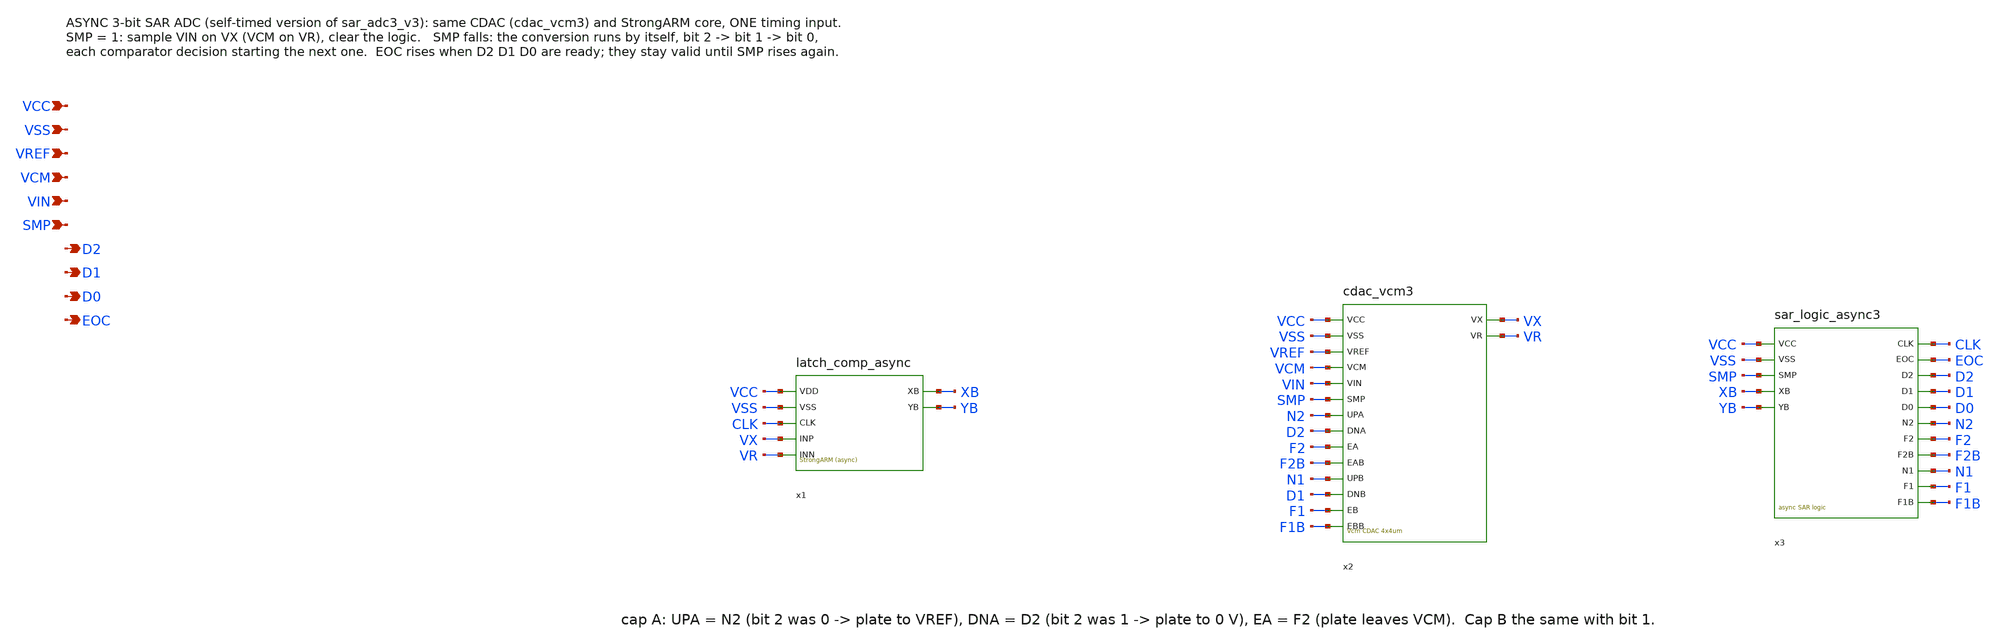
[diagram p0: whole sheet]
** sch_path: SAR_improved/sar_adc3_async.sch
**.subckt sar_adc3_async VCC VSS VREF VCM VIN SMP D2 D1 D0 EOC
*.ipin VCC
*.ipin VSS
*.ipin VREF
*.ipin VCM
*.ipin VIN
*.ipin SMP
*.opin D2
*.opin D1
*.opin D0
*.opin EOC
x1 VCC VSS CLK VX VR XB YB latch_comp_async
x2 VCC VSS VREF VCM VIN SMP N2 D2 F2 F2B N1 D1 F1 F1B VX VR cdac_vcm3
x3 VCC VSS SMP XB YB CLK EOC D2 D1 D0 N2 F2 F2B N1 F1 F1B sar_logic_async3
**.ends
.end
